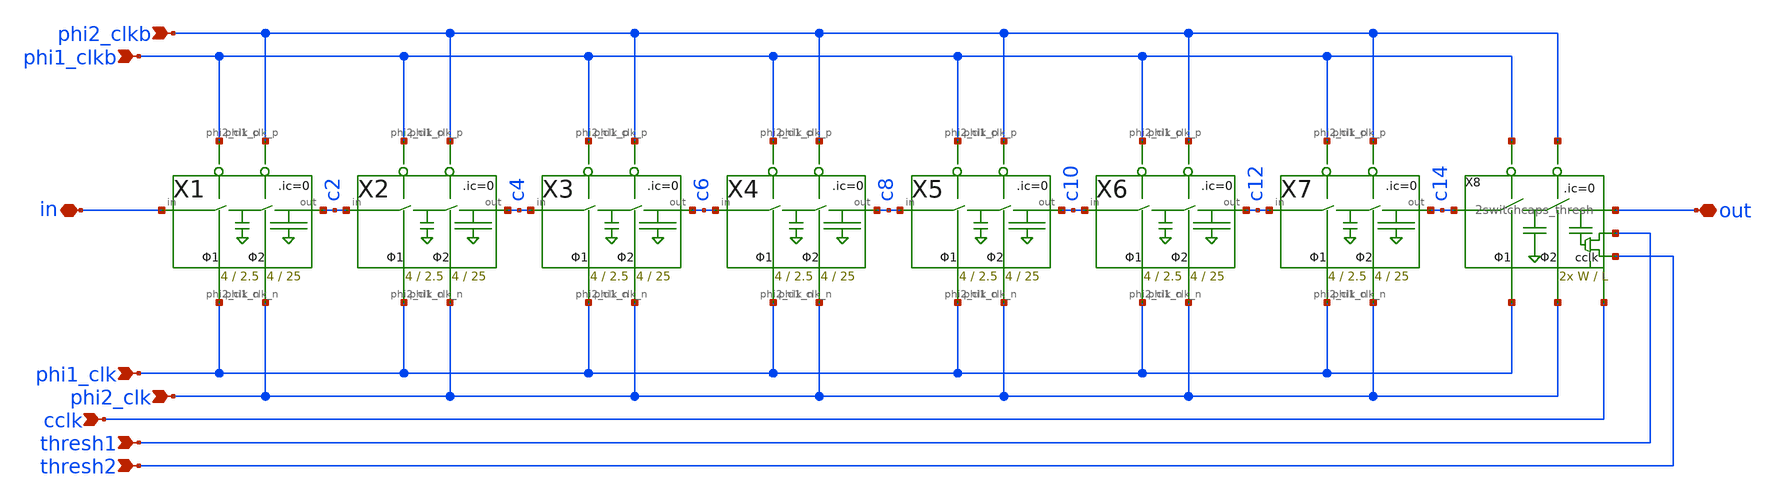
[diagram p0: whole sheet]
** sch_path: xschem/Switched_Caps/16switchcaps_2phi_thresh.sch
**.subckt 16switchcaps_2phi_thresh in out phi2_clkb phi1_clkb phi2_clk phi1_clk thresh1 cclk thresh2
*.iopin in
*.iopin out
*.ipin phi2_clkb
*.ipin phi1_clkb
*.ipin phi2_clk
*.ipin phi1_clk
*.ipin thresh1
*.ipin cclk
*.ipin thresh2
X1 in c2 phi2_clk phi1_clk phi1_clkb phi2_clkb 2switchcaps Wcap1=4 Lcap1=2.5 Wcap2=4 Lcap2=25
X2 c2 c4 phi2_clk phi1_clk phi1_clkb phi2_clkb 2switchcaps Wcap1=4 Lcap1=2.5 Wcap2=4 Lcap2=25
X3 c4 c6 phi2_clk phi1_clk phi1_clkb phi2_clkb 2switchcaps Wcap1=4 Lcap1=2.5 Wcap2=4 Lcap2=25
X4 c6 c8 phi2_clk phi1_clk phi1_clkb phi2_clkb 2switchcaps Wcap1=4 Lcap1=2.5 Wcap2=4 Lcap2=25
X5 c8 c10 phi2_clk phi1_clk phi1_clkb phi2_clkb 2switchcaps Wcap1=4 Lcap1=2.5 Wcap2=4 Lcap2=25
X6 c10 c12 phi2_clk phi1_clk phi1_clkb phi2_clkb 2switchcaps Wcap1=4 Lcap1=2.5 Wcap2=4 Lcap2=25
X7 c12 c14 phi2_clk phi1_clk phi1_clkb phi2_clkb 2switchcaps Wcap1=4 Lcap1=2.5 Wcap2=4 Lcap2=25
X8 c14 out phi2_clk phi1_clk phi1_clkb phi2_clkb thresh2 cclk thresh1 2switchcaps_thresh Wcap=W
+ Lcap=L
**.ends
.end
